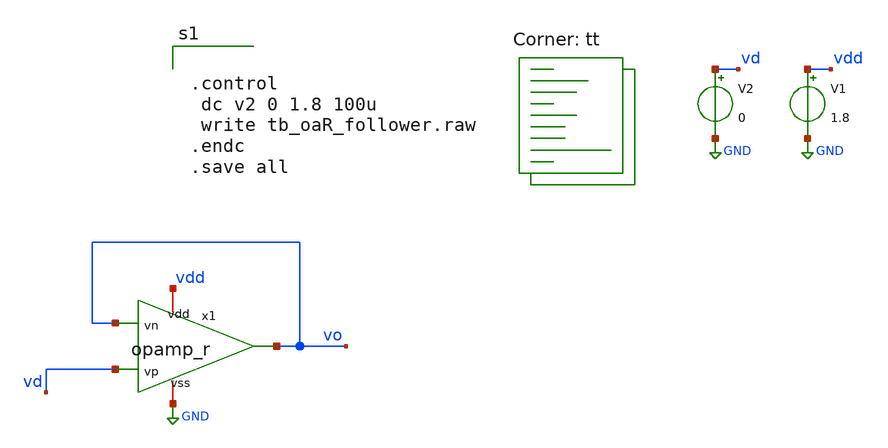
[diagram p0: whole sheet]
** sch_path: designs/subcells/tb_opampr/tb_oaR_follower.sch
**.subckt tb_oaR_follower
V1 vdd GND 1.8
V2 vd GND 0
x1 vdd vo vo vd GND opamp_r
**** begin user architecture code


.control
 dc v2 0 1.8 100u
 write tb_oaR_follower.raw
.endc
.save all

.lib $::SKYWATER_MODELS/sky130.lib.spice tt
**** end user architecture code
**.ends

* expanding   symbol:  /foss/designs/spike_130/designs/subcells/core_opampr/opamp_r.sym # of pins=5
** sym_path: designs/subcells/core_opampr/opamp_r.sym
** sch_path: designs/subcells/core_opampr/opamp_r.sch
.subckt opamp_r vdd vn vout vp vss
*.iopin vdd
*.opin vout
*.ipin vp
*.iopin vss
*.ipin vn
I0 vdd net3 10u
XM9 net1 vp net2 vss sky130_fd_pr__nfet_01v8 L=0.15 W=9 nf=2 ad='int((2 + 1)/2) * 9 / 2 * 0.29' as='int((2 + 2)/2) * 9 / 2 * 0.29'
+ pd='2*int((2 + 1)/2) * (9 / 2 + 0.29)' ps='2*int((2 + 2)/2) * (9 / 2 + 0.29)' nrd='0.29 / 9 ' nrs='0.29 / 9 '
+ sa=0 sb=0 sd=0 mult=12 m=12
XM4 net1 net1 vdd vdd sky130_fd_pr__pfet_01v8 L=0.35 W=1.3 nf=1 ad='int((nf+1)/2) * W/nf * 0.29' as='int((nf+2)/2) * W/nf * 0.29'
+ pd='2*int((nf+1)/2) * (W/nf + 0.29)' ps='2*int((nf+2)/2) * (W/nf + 0.29)' nrd='0.29 / W' nrs='0.29 / W'
+ sa=0 sb=0 sd=0 mult=2 m=2
XM5 net1 vout vdd vdd sky130_fd_pr__pfet_01v8 L=0.35 W=1.3 nf=1 ad='int((nf+1)/2) * W/nf * 0.29' as='int((nf+2)/2) * W/nf * 0.29'
+ pd='2*int((nf+1)/2) * (W/nf + 0.29)' ps='2*int((nf+2)/2) * (W/nf + 0.29)' nrd='0.29 / W' nrs='0.29 / W'
+ sa=0 sb=0 sd=0 mult=2 m=2
XM6 vout net1 vdd vdd sky130_fd_pr__pfet_01v8 L=0.35 W=1.3 nf=1 ad='int((nf+1)/2) * W/nf * 0.29' as='int((nf+2)/2) * W/nf * 0.29'
+ pd='2*int((nf+1)/2) * (W/nf + 0.29)' ps='2*int((nf+2)/2) * (W/nf + 0.29)' nrd='0.29 / W' nrs='0.29 / W'
+ sa=0 sb=0 sd=0 mult=2 m=2
XM7 vout vout vdd vdd sky130_fd_pr__pfet_01v8 L=0.35 W=1.3 nf=1 ad='int((nf+1)/2) * W/nf * 0.29' as='int((nf+2)/2) * W/nf * 0.29'
+ pd='2*int((nf+1)/2) * (W/nf + 0.29)' ps='2*int((nf+2)/2) * (W/nf + 0.29)' nrd='0.29 / W' nrs='0.29 / W'
+ sa=0 sb=0 sd=0 mult=2 m=2
XM1 vout vn net2 vss sky130_fd_pr__nfet_01v8 L=0.15 W=9 nf=2 ad='int((2 + 1)/2) * 9 / 2 * 0.29' as='int((2 + 2)/2) * 9 / 2 * 0.29'
+ pd='2*int((2 + 1)/2) * (9 / 2 + 0.29)' ps='2*int((2 + 2)/2) * (9 / 2 + 0.29)' nrd='0.29 / 9 ' nrs='0.29 / 9 '
+ sa=0 sb=0 sd=0 mult=12 m=12
XM2 net2 net3 vss vss sky130_fd_pr__nfet_01v8 L=3 W=1.5 nf=2 ad='int((2 + 1)/2) * 1.5 / 2 * 0.29' as='int((2 + 2)/2) * 1.5 / 2 * 0.29'
+ pd='2*int((2 + 1)/2) * (1.5 / 2 + 0.29)' ps='2*int((2 + 2)/2) * (1.5 / 2 + 0.29)' nrd='0.29 / 1.5 ' nrs='0.29 / 1.5 '
+ sa=0 sb=0 sd=0 mult=3 m=3
XM3 net3 net3 vss vss sky130_fd_pr__nfet_01v8 L=3 W=1.5 nf=2 ad='int((2 + 1)/2) * 1.5 / 2 * 0.29' as='int((2 + 2)/2) * 1.5 / 2 * 0.29'
+ pd='2*int((2 + 1)/2) * (1.5 / 2 + 0.29)' ps='2*int((2 + 2)/2) * (1.5 / 2 + 0.29)' nrd='0.29 / 1.5 ' nrs='0.29 / 1.5 '
+ sa=0 sb=0 sd=0 mult=3 m=3
.ends

.GLOBAL GND
.end
